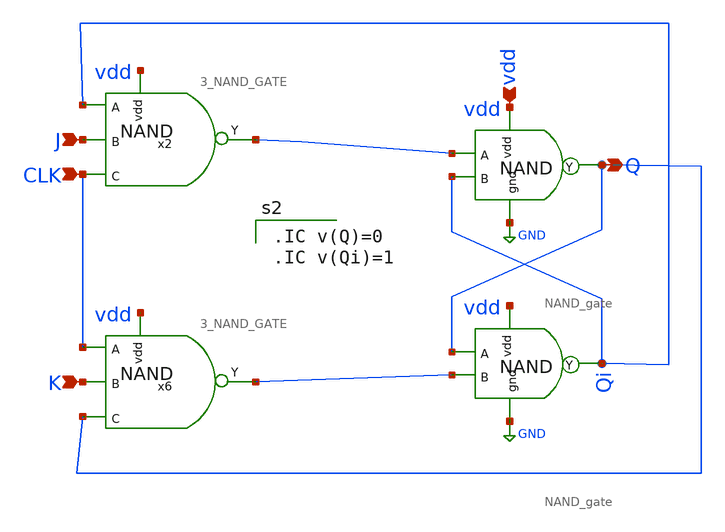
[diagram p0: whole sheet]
** sch_path: Circuit Files/circuits/circuits/JK_FF.sch
**.subckt JK_FF J vdd Q CLK K
*.ipin J
*.ipin vdd
*.opin Q
*.ipin CLK
*.ipin K
x3 vdd Q net1 Qi GND NAND_gate
x5 vdd Qi Q net2 GND NAND_gate
x2 vdd net1 Qi J CLK 3_NAND_GATE
x6 vdd net2 CLK K Q 3_NAND_GATE
**** begin user architecture code

.IC v(Q)=0
.IC v(Qi)=1


**** end user architecture code
**.ends

* expanding   symbol:  daVLSI_World/gates/NAND_gate.sym # of pins=5
** sym_path: Circuit Files/Logic gate design using MOSFETS/gates/NAND_gate.sym
** sch_path: Circuit Files/Logic gate design using MOSFETS/gates/NAND_gate.sch
.subckt NAND_gate vdd Y A B gnd
*.ipin A
*.ipin B
*.opin Y
*.ipin vdd
*.ipin gnd
XM1 Y A net1 gnd sky130_fd_pr__nfet_01v8 L=0.15 W=1 nf=1 ad='int((nf+1)/2) * W/nf * 0.29' as='int((nf+2)/2) * W/nf * 0.29'
+ pd='2*int((nf+1)/2) * (W/nf + 0.29)' ps='2*int((nf+2)/2) * (W/nf + 0.29)' nrd='0.29 / W' nrs='0.29 / W'
+ sa=0 sb=0 sd=0 mult=1 m=1
XM2 net1 B gnd gnd sky130_fd_pr__nfet_01v8 L=0.15 W=1 nf=1 ad='int((nf+1)/2) * W/nf * 0.29' as='int((nf+2)/2) * W/nf * 0.29'
+ pd='2*int((nf+1)/2) * (W/nf + 0.29)' ps='2*int((nf+2)/2) * (W/nf + 0.29)' nrd='0.29 / W' nrs='0.29 / W'
+ sa=0 sb=0 sd=0 mult=1 m=1
XM3 Y A vdd vdd sky130_fd_pr__pfet_01v8 L=0.15 W=2 nf=1 ad='int((nf+1)/2) * W/nf * 0.29' as='int((nf+2)/2) * W/nf * 0.29'
+ pd='2*int((nf+1)/2) * (W/nf + 0.29)' ps='2*int((nf+2)/2) * (W/nf + 0.29)' nrd='0.29 / W' nrs='0.29 / W'
+ sa=0 sb=0 sd=0 mult=1 m=1
XM4 Y B vdd vdd sky130_fd_pr__pfet_01v8 L=0.15 W=2 nf=1 ad='int((nf+1)/2) * W/nf * 0.29' as='int((nf+2)/2) * W/nf * 0.29'
+ pd='2*int((nf+1)/2) * (W/nf + 0.29)' ps='2*int((nf+2)/2) * (W/nf + 0.29)' nrd='0.29 / W' nrs='0.29 / W'
+ sa=0 sb=0 sd=0 mult=1 m=1
.ends


* expanding   symbol:  daVLSI_World/gates/3_NAND_GATE.sym # of pins=5
** sym_path: Circuit Files/Logic gate design using MOSFETS/gates/3_NAND_GATE.sym
** sch_path: Circuit Files/Logic gate design using MOSFETS/gates/3_NAND_GATE.sch
.subckt 3_NAND_GATE vdd Y A B C
*.ipin A
*.ipin B
*.opin Y
*.ipin vdd
*.ipin C
XM1 Y A net1 GND sky130_fd_pr__nfet_01v8 L=0.15 W=1 nf=1 ad='int((nf+1)/2) * W/nf * 0.29' as='int((nf+2)/2) * W/nf * 0.29'
+ pd='2*int((nf+1)/2) * (W/nf + 0.29)' ps='2*int((nf+2)/2) * (W/nf + 0.29)' nrd='0.29 / W' nrs='0.29 / W'
+ sa=0 sb=0 sd=0 mult=1 m=1
XM2 net1 B net2 GND sky130_fd_pr__nfet_01v8 L=0.15 W=1 nf=1 ad='int((nf+1)/2) * W/nf * 0.29' as='int((nf+2)/2) * W/nf * 0.29'
+ pd='2*int((nf+1)/2) * (W/nf + 0.29)' ps='2*int((nf+2)/2) * (W/nf + 0.29)' nrd='0.29 / W' nrs='0.29 / W'
+ sa=0 sb=0 sd=0 mult=1 m=1
XM3 Y A vdd vdd sky130_fd_pr__pfet_01v8 L=0.15 W=2 nf=1 ad='int((nf+1)/2) * W/nf * 0.29' as='int((nf+2)/2) * W/nf * 0.29'
+ pd='2*int((nf+1)/2) * (W/nf + 0.29)' ps='2*int((nf+2)/2) * (W/nf + 0.29)' nrd='0.29 / W' nrs='0.29 / W'
+ sa=0 sb=0 sd=0 mult=1 m=1
XM4 Y B vdd vdd sky130_fd_pr__pfet_01v8 L=0.15 W=2 nf=1 ad='int((nf+1)/2) * W/nf * 0.29' as='int((nf+2)/2) * W/nf * 0.29'
+ pd='2*int((nf+1)/2) * (W/nf + 0.29)' ps='2*int((nf+2)/2) * (W/nf + 0.29)' nrd='0.29 / W' nrs='0.29 / W'
+ sa=0 sb=0 sd=0 mult=1 m=1
XM5 net2 C GND GND sky130_fd_pr__nfet_01v8 L=0.15 W=1 nf=1 ad='int((nf+1)/2) * W/nf * 0.29' as='int((nf+2)/2) * W/nf * 0.29'
+ pd='2*int((nf+1)/2) * (W/nf + 0.29)' ps='2*int((nf+2)/2) * (W/nf + 0.29)' nrd='0.29 / W' nrs='0.29 / W'
+ sa=0 sb=0 sd=0 mult=1 m=1
XM6 Y C vdd vdd sky130_fd_pr__pfet_01v8 L=0.15 W=2 nf=1 ad='int((nf+1)/2) * W/nf * 0.29' as='int((nf+2)/2) * W/nf * 0.29'
+ pd='2*int((nf+1)/2) * (W/nf + 0.29)' ps='2*int((nf+2)/2) * (W/nf + 0.29)' nrd='0.29 / W' nrs='0.29 / W'
+ sa=0 sb=0 sd=0 mult=1 m=1
.ends

.GLOBAL GND
.end
